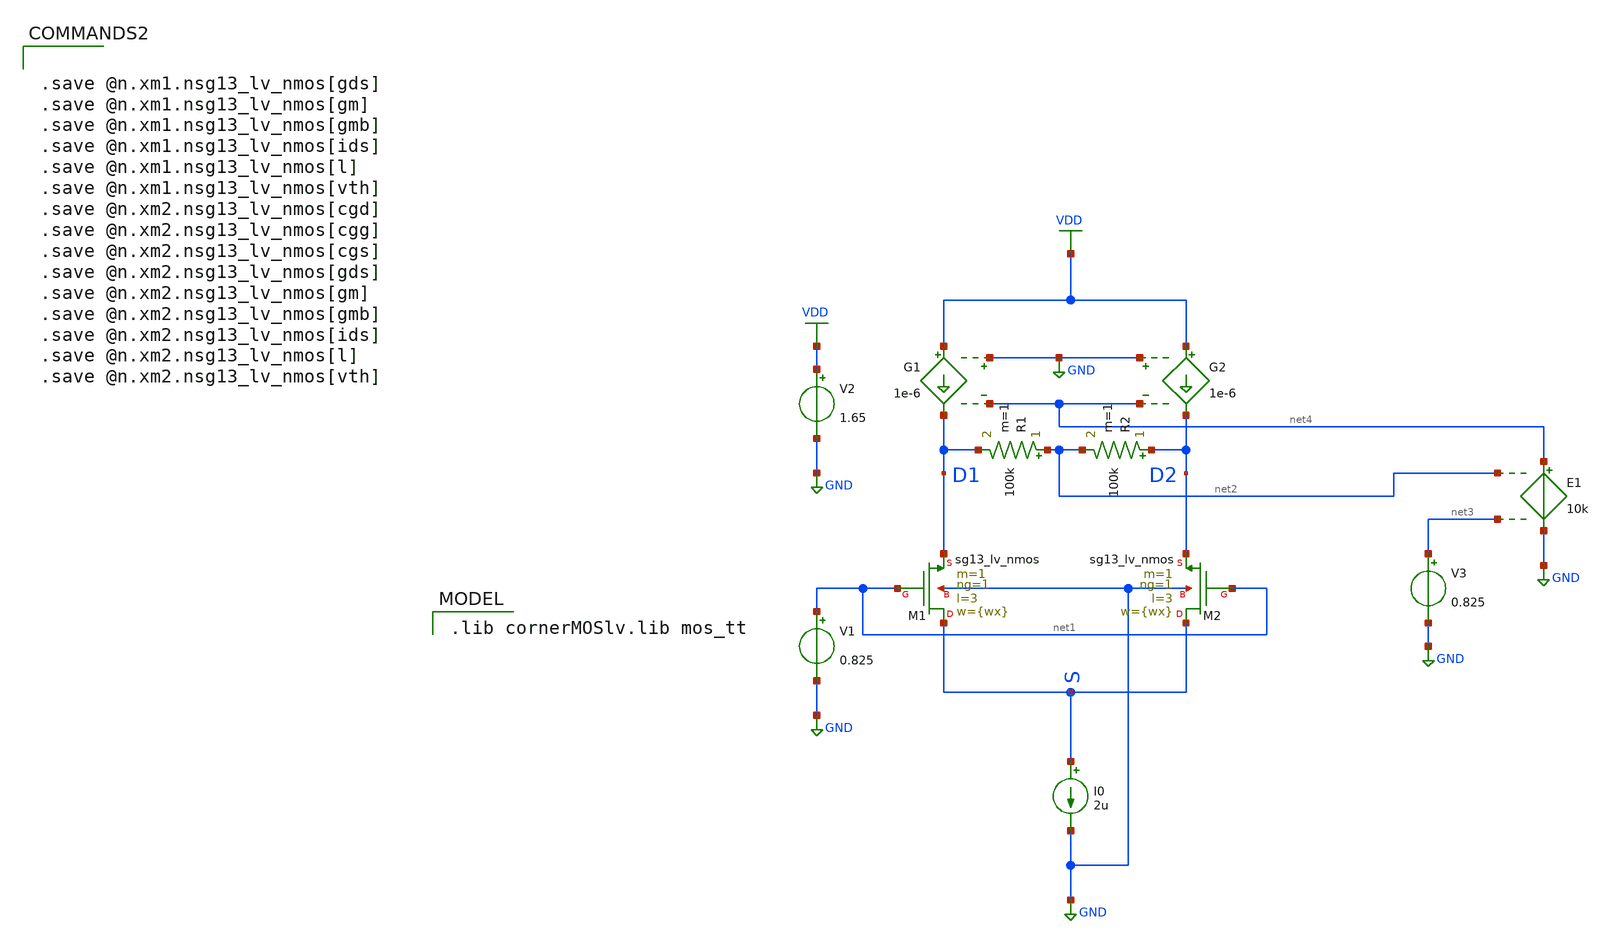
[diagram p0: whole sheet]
** sch_path: VLSI25/submitted_notebooks/Wrøngm/Schematics/Diff-amp_test.sch
**.subckt Diff-amp_test
XM1 S net1 D1 GND sg13_lv_nmos w={wx} l=3 ng=1 m=1 mm_ok=1
XM2 S net1 D2 GND sg13_lv_nmos w={wx} l=3 ng=1 m=1 mm_ok=1
I0 S GND 2u
V1 net1 GND 0.825
V2 VDD GND 1.65
E1 net4 GND net2 net3 10k
R1 net2 D1 100k m=1
R2 D2 net2 100k m=1
V3 net3 GND 0.825
G1 VDD D1 GND net4 1e-6
G2 VDD D2 GND net4 1e-6
**** begin user architecture code


* ngspice commands
.param wx=1u
.options savecurrents

.control
  let start_w = 0.5u
  let stop_w = 20u
  let delta_w = 0.1u
  let w_act = start_w

  while w_act le stop_w
    let wx = w_act

    alterparam wx = $&w_act
    reset
    save all

    dc v1 0 1.65 1m
    wrdata /foss/designs/CAC/5T-OTA/Diff-amp_test_3.txt v(D1) v(D2) v(S) @n.xm1.nsg13_lv_nmos[gm]
+ @n.xm1.nsg13_lv_nmos[gds] @n.xm1.nsg13_lv_nmos[vgs] @n.xm1.nsg13_lv_nmos[vth] @n.xm1.nsg13_lv_nmos[vsat]
+ @n.xm1.nsg13_lv_nmos[vds] @n.xm1.nsg13_lv_nmos[ids] @n.xm1.nsg13_lv_nmos[cgg]
    let w_act = w_act + delta_w
    set appendwrite
  end
.endc




.save @n.xm1.nsg13_lv_nmos[gds]
.save @n.xm1.nsg13_lv_nmos[gm]
.save @n.xm1.nsg13_lv_nmos[gmb]
.save @n.xm1.nsg13_lv_nmos[ids]
.save @n.xm1.nsg13_lv_nmos[l]
.save @n.xm1.nsg13_lv_nmos[vth]
.save @n.xm2.nsg13_lv_nmos[cgd]
.save @n.xm2.nsg13_lv_nmos[cgg]
.save @n.xm2.nsg13_lv_nmos[cgs]
.save @n.xm2.nsg13_lv_nmos[gds]
.save @n.xm2.nsg13_lv_nmos[gm]
.save @n.xm2.nsg13_lv_nmos[gmb]
.save @n.xm2.nsg13_lv_nmos[ids]
.save @n.xm2.nsg13_lv_nmos[l]
.save @n.xm2.nsg13_lv_nmos[vth]


 .lib cornerMOSlv.lib mos_tt

**** end user architecture code
**.ends
.GLOBAL GND
.GLOBAL VDD
.end
